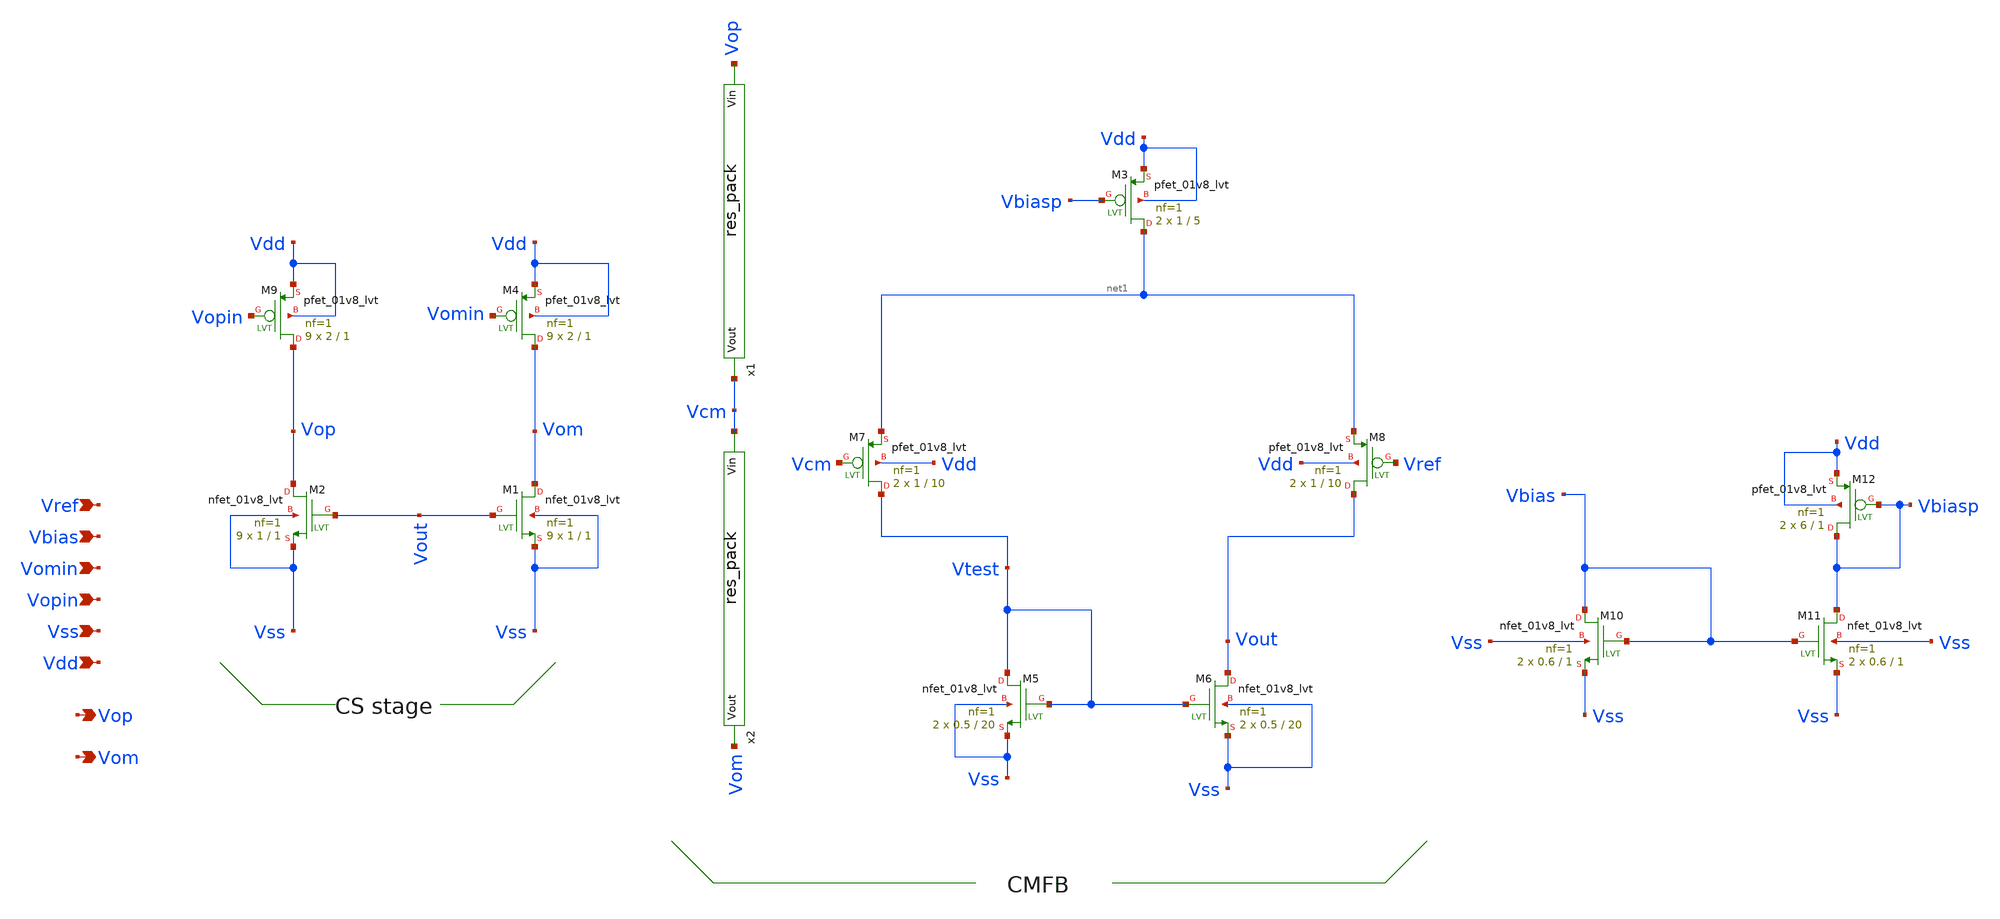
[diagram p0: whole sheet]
** sch_path: src/Opamp_Design/src/Common_source_stage.sch
**.subckt Common_source_stage Vdd Vop Vss Vom Vopin Vomin Vbias Vref
*.ipin Vdd
*.opin Vop
*.ipin Vss
*.opin Vom
*.ipin Vopin
*.ipin Vomin
*.ipin Vbias
*.ipin Vref
XM9 Vop Vopin Vdd Vdd sky130_fd_pr__pfet_01v8_lvt L=1 W=2 nf=1 ad='int((nf+1)/2) * W/nf * 0.29' as='int((nf+2)/2) * W/nf * 0.29'
+ pd='2*int((nf+1)/2) * (W/nf + 0.29)' ps='2*int((nf+2)/2) * (W/nf + 0.29)' nrd='0.29 / W' nrs='0.29 / W'
+ sa=0 sb=0 sd=0 mult=9 m=9
XM4 Vom Vomin Vdd Vdd sky130_fd_pr__pfet_01v8_lvt L=1 W=2 nf=1 ad='int((nf+1)/2) * W/nf * 0.29' as='int((nf+2)/2) * W/nf * 0.29'
+ pd='2*int((nf+1)/2) * (W/nf + 0.29)' ps='2*int((nf+2)/2) * (W/nf + 0.29)' nrd='0.29 / W' nrs='0.29 / W'
+ sa=0 sb=0 sd=0 mult=9 m=9
XM2 Vop Vout Vss Vss sky130_fd_pr__nfet_01v8_lvt L=1 W=1 nf=1 ad='int((nf+1)/2) * W/nf * 0.29' as='int((nf+2)/2) * W/nf * 0.29'
+ pd='2*int((nf+1)/2) * (W/nf + 0.29)' ps='2*int((nf+2)/2) * (W/nf + 0.29)' nrd='0.29 / W' nrs='0.29 / W'
+ sa=0 sb=0 sd=0 mult=9 m=9
XM1 Vom Vout Vss Vss sky130_fd_pr__nfet_01v8_lvt L=1 W=1 nf=1 ad='int((nf+1)/2) * W/nf * 0.29' as='int((nf+2)/2) * W/nf * 0.29'
+ pd='2*int((nf+1)/2) * (W/nf + 0.29)' ps='2*int((nf+2)/2) * (W/nf + 0.29)' nrd='0.29 / W' nrs='0.29 / W'
+ sa=0 sb=0 sd=0 mult=9 m=9
XM3 net1 Vbiasp Vdd Vdd sky130_fd_pr__pfet_01v8_lvt L=5 W=1 nf=1 ad='int((nf+1)/2) * W/nf * 0.29' as='int((nf+2)/2) * W/nf * 0.29'
+ pd='2*int((nf+1)/2) * (W/nf + 0.29)' ps='2*int((nf+2)/2) * (W/nf + 0.29)' nrd='0.29 / W' nrs='0.29 / W'
+ sa=0 sb=0 sd=0 mult=2 m=2
XM7 Vtest Vcm net1 Vdd sky130_fd_pr__pfet_01v8_lvt L=10 W=1 nf=1 ad='int((nf+1)/2) * W/nf * 0.29' as='int((nf+2)/2) * W/nf * 0.29'
+ pd='2*int((nf+1)/2) * (W/nf + 0.29)' ps='2*int((nf+2)/2) * (W/nf + 0.29)' nrd='0.29 / W' nrs='0.29 / W'
+ sa=0 sb=0 sd=0 mult=2 m=2
XM8 Vout Vref net1 Vdd sky130_fd_pr__pfet_01v8_lvt L=10 W=1 nf=1 ad='int((nf+1)/2) * W/nf * 0.29' as='int((nf+2)/2) * W/nf * 0.29'
+ pd='2*int((nf+1)/2) * (W/nf + 0.29)' ps='2*int((nf+2)/2) * (W/nf + 0.29)' nrd='0.29 / W' nrs='0.29 / W'
+ sa=0 sb=0 sd=0 mult=2 m=2
XM5 Vtest Vtest Vss Vss sky130_fd_pr__nfet_01v8_lvt L=20 W=0.5 nf=1 ad='int((nf+1)/2) * W/nf * 0.29'
+ as='int((nf+2)/2) * W/nf * 0.29' pd='2*int((nf+1)/2) * (W/nf + 0.29)' ps='2*int((nf+2)/2) * (W/nf + 0.29)'
+ nrd='0.29 / W' nrs='0.29 / W' sa=0 sb=0 sd=0 mult=2 m=2
XM6 Vout Vtest Vss Vss sky130_fd_pr__nfet_01v8_lvt L=20 W=0.5 nf=1 ad='int((nf+1)/2) * W/nf * 0.29' as='int((nf+2)/2) * W/nf * 0.29'
+ pd='2*int((nf+1)/2) * (W/nf + 0.29)' ps='2*int((nf+2)/2) * (W/nf + 0.29)' nrd='0.29 / W' nrs='0.29 / W'
+ sa=0 sb=0 sd=0 mult=2 m=2
x1 Vop Vcm res_pack
x2 Vcm Vom res_pack
XM10 Vbias Vbias Vss Vss sky130_fd_pr__nfet_01v8_lvt L=1 W=0.6 nf=1 ad='int((nf+1)/2) * W/nf * 0.29'
+ as='int((nf+2)/2) * W/nf * 0.29' pd='2*int((nf+1)/2) * (W/nf + 0.29)' ps='2*int((nf+2)/2) * (W/nf + 0.29)'
+ nrd='0.29 / W' nrs='0.29 / W' sa=0 sb=0 sd=0 mult=2 m=2
XM11 Vbiasp Vbias Vss Vss sky130_fd_pr__nfet_01v8_lvt L=1 W=0.6 nf=1 ad='int((nf+1)/2) * W/nf * 0.29'
+ as='int((nf+2)/2) * W/nf * 0.29' pd='2*int((nf+1)/2) * (W/nf + 0.29)' ps='2*int((nf+2)/2) * (W/nf + 0.29)'
+ nrd='0.29 / W' nrs='0.29 / W' sa=0 sb=0 sd=0 mult=2 m=2
XM12 Vbiasp Vbiasp Vdd Vdd sky130_fd_pr__pfet_01v8_lvt L=1 W=6 nf=1 ad='int((nf+1)/2) * W/nf * 0.29'
+ as='int((nf+2)/2) * W/nf * 0.29' pd='2*int((nf+1)/2) * (W/nf + 0.29)' ps='2*int((nf+2)/2) * (W/nf + 0.29)'
+ nrd='0.29 / W' nrs='0.29 / W' sa=0 sb=0 sd=0 mult=2 m=2
**.ends

* expanding   symbol:  /foss/designs/FYP/Sky130_Design/Opamp_Design/src/res_pack.sym # of pins=2
** sym_path: src/Opamp_Design/src/res_pack.sym
** sch_path: src/Opamp_Design/src/res_pack.sch
.subckt res_pack Vin Vout
*.ipin Vin
*.opin Vout
XR1 net4 Vin sky130_fd_pr__res_generic_po W=0.5 L=40 m=1
XR2 net5 net4 sky130_fd_pr__res_generic_po W=0.5 L=40 m=1
XR3 net6 net5 sky130_fd_pr__res_generic_po W=0.5 L=40 m=1
XR4 net7 net6 sky130_fd_pr__res_generic_po W=0.5 L=40 m=1
XR5 net1 net7 sky130_fd_pr__res_generic_po W=0.5 L=40 m=1
XR6 net8 net2 sky130_fd_pr__res_generic_po W=0.5 L=40 m=1
XR7 net9 net8 sky130_fd_pr__res_generic_po W=0.5 L=40 m=1
XR8 net10 net9 sky130_fd_pr__res_generic_po W=0.5 L=40 m=1
XR9 net11 net10 sky130_fd_pr__res_generic_po W=0.5 L=40 m=1
XR10 net1 net11 sky130_fd_pr__res_generic_po W=0.5 L=40 m=1
XR11 net12 net2 sky130_fd_pr__res_generic_po W=0.5 L=40 m=1
XR12 net13 net12 sky130_fd_pr__res_generic_po W=0.5 L=40 m=1
XR13 net14 net13 sky130_fd_pr__res_generic_po W=0.5 L=40 m=1
XR14 net15 net14 sky130_fd_pr__res_generic_po W=0.5 L=40 m=1
XR16 net16 Vout sky130_fd_pr__res_generic_po W=0.5 L=40 m=1
XR17 net17 net16 sky130_fd_pr__res_generic_po W=0.5 L=40 m=1
XR18 net18 net17 sky130_fd_pr__res_generic_po W=0.5 L=40 m=1
XR19 net19 net18 sky130_fd_pr__res_generic_po W=0.5 L=40 m=1
XR20 net3 net19 sky130_fd_pr__res_generic_po W=0.5 L=40 m=1
XR15 net3 net15 sky130_fd_pr__res_generic_po W=0.5 L=40 m=1
.ends

.end
